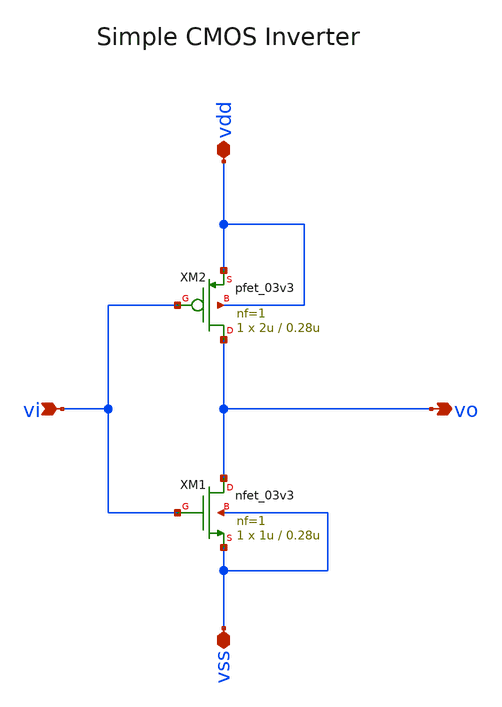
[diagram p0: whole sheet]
** sch_path: xschem/sar_adc/blocks/sample_hold/inv_sh.sch
**.subckt inv_sh vdd vi vo vss
*.iopin vdd
*.ipin vi
*.opin vo
*.iopin vss
XM1 vo vi vss vss nfet_03v3 L=0.28u W=1u nf=1 ad='int((nf+1)/2) * W/nf * 0.18u' as='int((nf+2)/2) * W/nf * 0.18u'
+ pd='2*int((nf+1)/2) * (W/nf + 0.18u)' ps='2*int((nf+2)/2) * (W/nf + 0.18u)' nrd='0.18u / W' nrs='0.18u / W'
+ sa=0 sb=0 sd=0 m=1
XM2 vo vi vdd vdd pfet_03v3 L=0.28u W=2u nf=1 ad='int((nf+1)/2) * W/nf * 0.18u' as='int((nf+2)/2) * W/nf * 0.18u'
+ pd='2*int((nf+1)/2) * (W/nf + 0.18u)' ps='2*int((nf+2)/2) * (W/nf + 0.18u)' nrd='0.18u / W' nrs='0.18u / W'
+ sa=0 sb=0 sd=0 m=1
**.ends
.end
